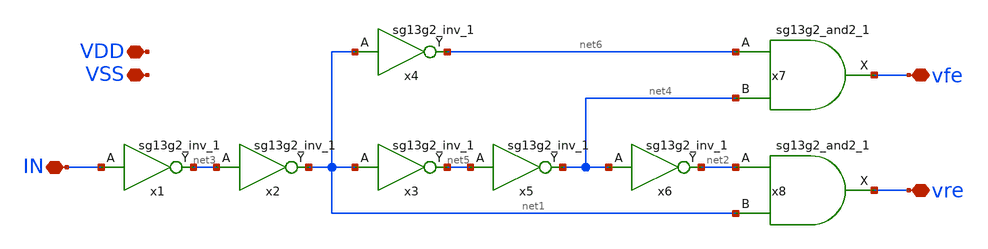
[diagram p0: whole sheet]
** sch_path: xschem/Floating_Gate/DIGITAL.sch
**.subckt DIGITAL IN VDD VSS vfe vre
*.iopin IN
*.iopin VDD
*.iopin VSS
*.iopin vfe
*.iopin vre
x1 net3 IN VDD VSS sg13g2_inv_1
x2 net1 net3 VDD VSS sg13g2_inv_1
x3 net5 net1 VDD VSS sg13g2_inv_1
x5 net4 net5 VDD VSS sg13g2_inv_1
x6 net2 net4 VDD VSS sg13g2_inv_1
x8 vre net2 net1 VDD VSS sg13g2_and2_1
x4 net6 net1 VDD VSS sg13g2_inv_1
x7 vfe net6 net4 VDD VSS sg13g2_and2_1
**** begin user architecture code

.include sg13g2_stdcell.cdl

**** end user architecture code
**.ends

* expanding   symbol:  sg13g2_stdcells/sg13g2_inv_1.sym # of pins=2
** sym_path: sg13g2_stdcells/sg13g2_inv_1.sym
** sch_path: sg13g2_stdcells/sg13g2_inv_1.sch
.subckt sg13g2_inv_1 Y A VDD VSS
*.opin Y
*.ipin A
*.iopin VDD
*.iopin VSS
XM1 Y A VSS VSS sg13_lv_nmos w=740.00n l=130.00n ng=1 m=1 mm_ok=1
XM2 Y A VDD VDD sg13_lv_pmos w=1.12u l=130.00n ng=1 m=1 mm_ok=1
.ends


* expanding   symbol:  sg13g2_stdcells/sg13g2_and2_1.sym # of pins=3
** sym_path: sg13g2_stdcells/sg13g2_and2_1.sym
** sch_path: sg13g2_stdcells/sg13g2_and2_1.sch
.subckt sg13g2_and2_1 X A B VDD VSS
*.ipin A
*.ipin B
*.opin X
*.iopin VDD
*.iopin VSS
XM1 net1 A net2 VSS sg13_lv_nmos w=640.00n l=130.00n ng=1 m=1 mm_ok=1
XM2 net2 B VSS VSS sg13_lv_nmos w=640.00n l=130.00n ng=1 m=1 mm_ok=1
XM3 X net1 VSS VSS sg13_lv_nmos w=740.00n l=130.00n ng=1 m=1 mm_ok=1
XM4 net1 B VDD VDD sg13_lv_pmos w=840.00n l=130.00n ng=1 m=1 mm_ok=1
XM5 net1 A VDD VDD sg13_lv_pmos w=840.00n l=130.00n ng=1 m=1 mm_ok=1
XM6 X net1 VDD VDD sg13_lv_pmos w=1.12u l=130.00n ng=1 m=1 mm_ok=1
.ends

.end
